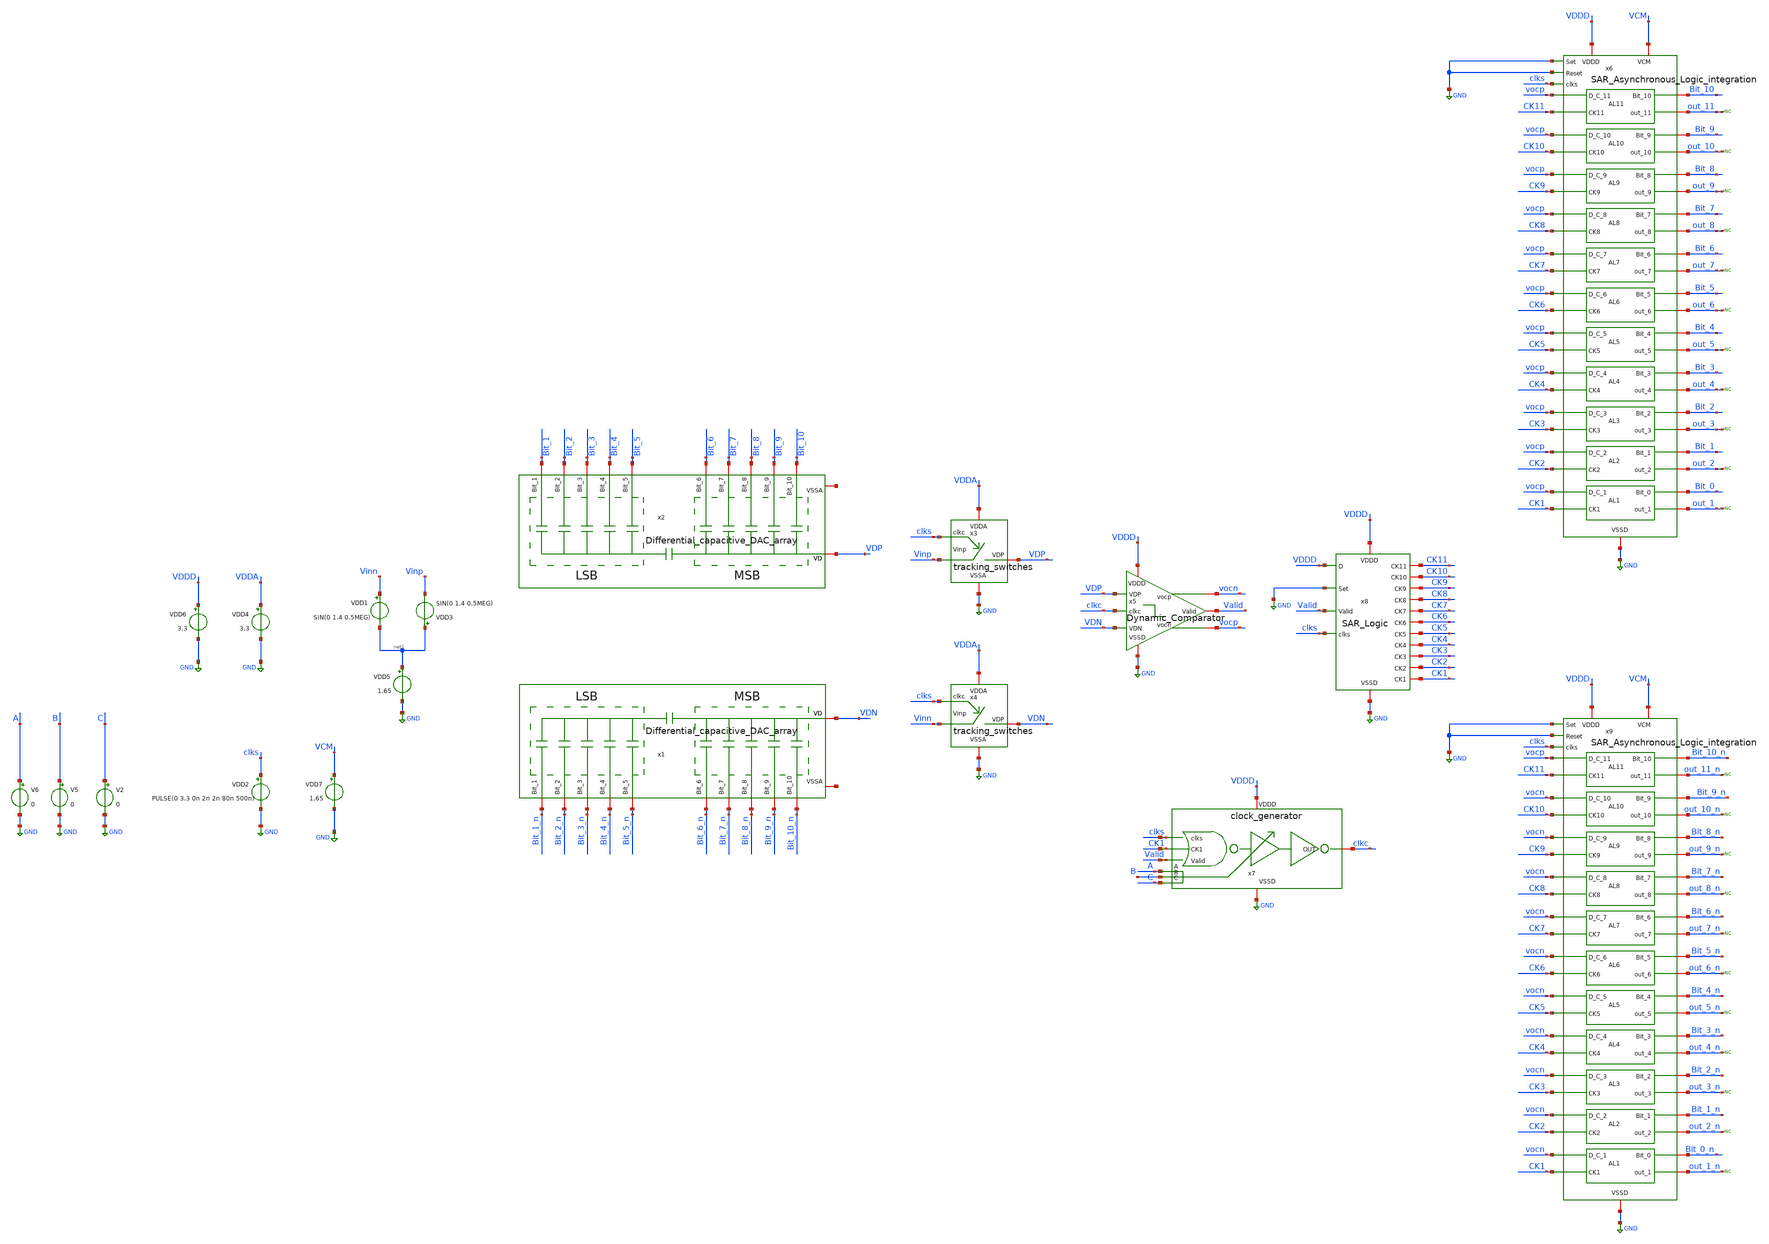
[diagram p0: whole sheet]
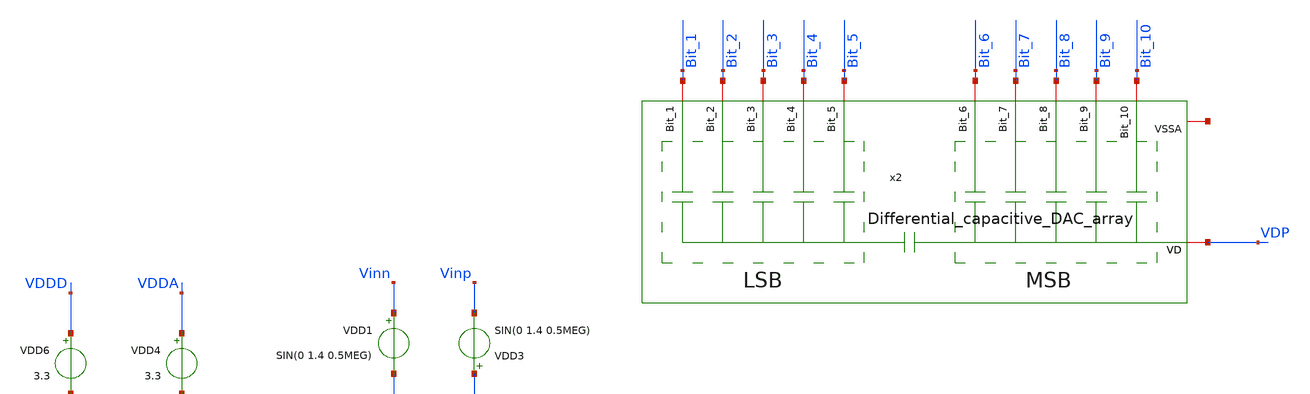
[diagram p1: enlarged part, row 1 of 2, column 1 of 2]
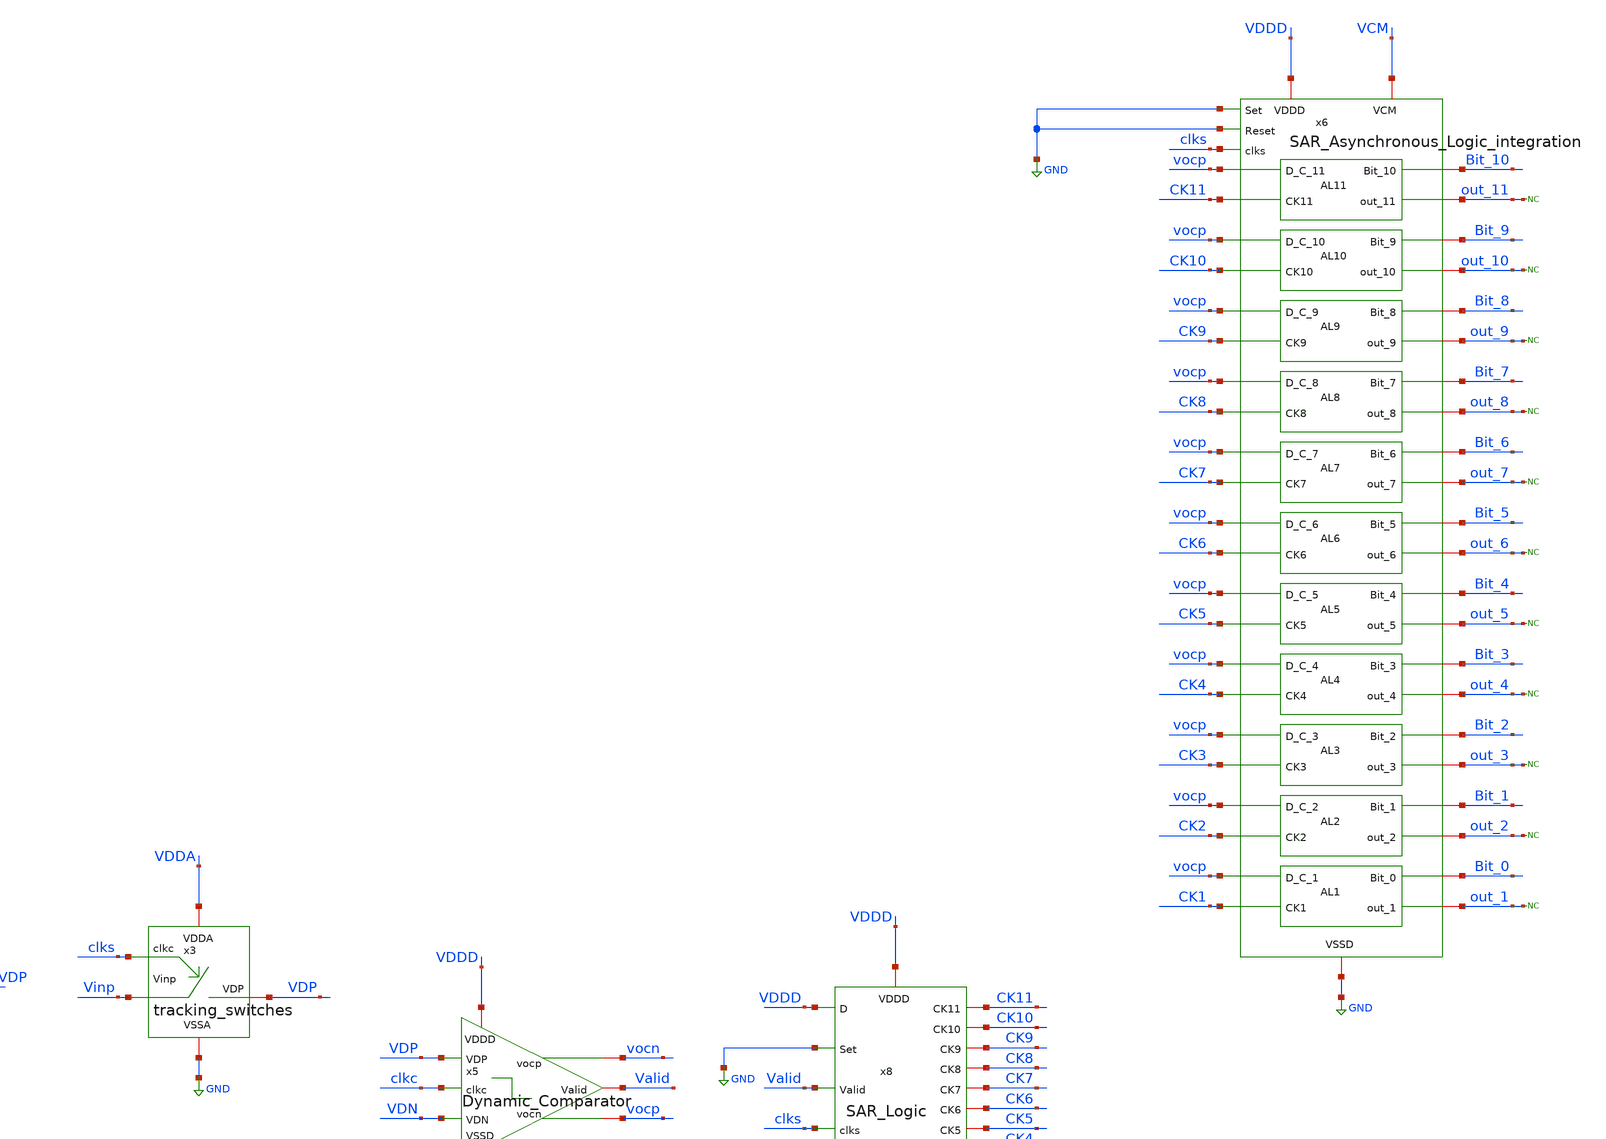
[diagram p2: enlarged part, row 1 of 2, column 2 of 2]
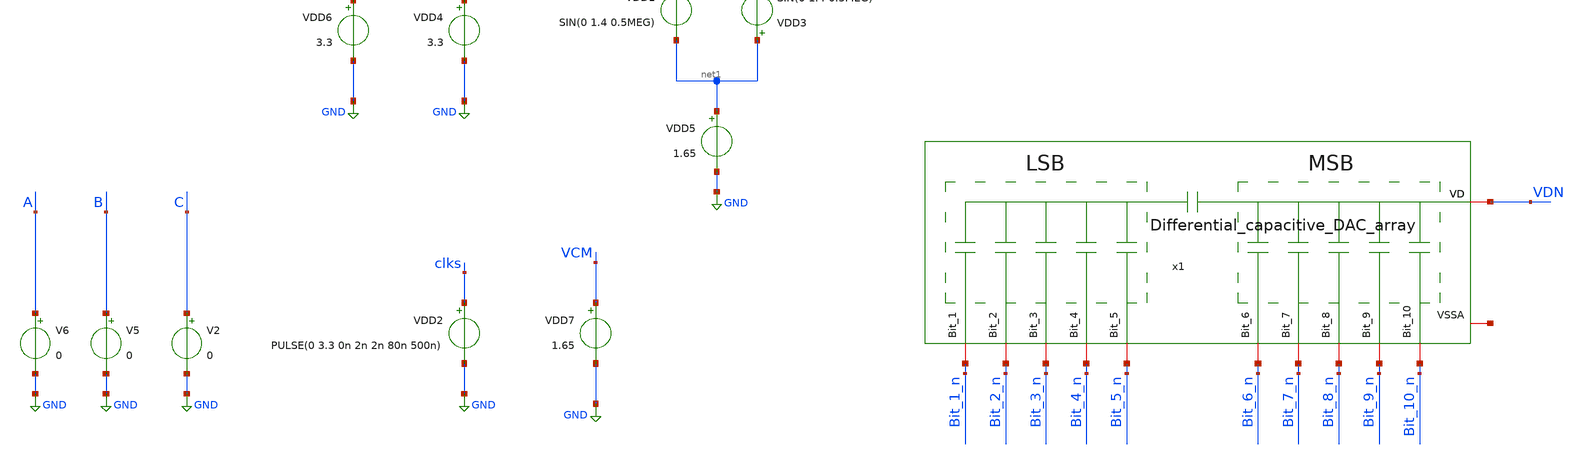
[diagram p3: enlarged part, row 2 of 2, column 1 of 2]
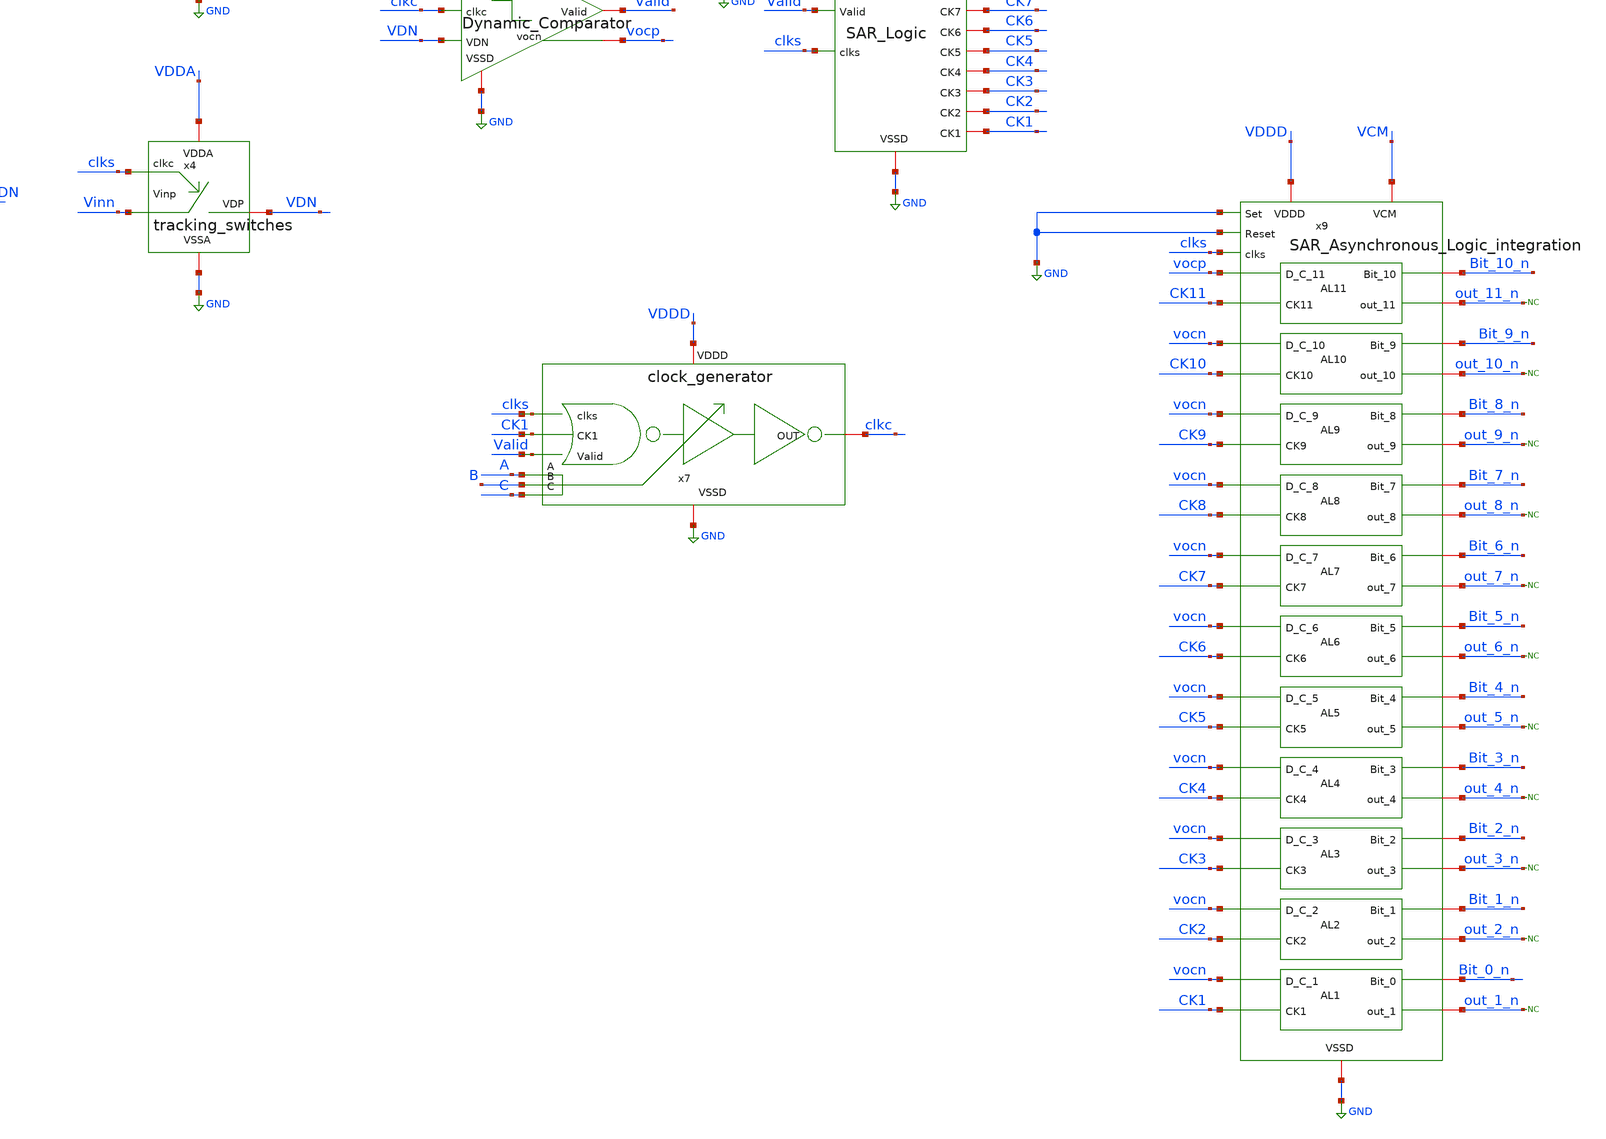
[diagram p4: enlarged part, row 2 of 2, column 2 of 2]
** sch_path: SAR_ADC/integration/integration_tb_bkp.sch
**.subckt integration_tb_bkp
x1 VDN Bit_3_n Bit_8_n Bit_5_n Bit_6_n Bit_7_n Bit_4_n Bit_9_n Bit_10_n Bit_2_n Bit_1_n net2
+ Differential_capacitive_DAC_array
x2 VDP Bit_3 Bit_8 Bit_5 Bit_6 Bit_7 Bit_4 Bit_9 Bit_10 Bit_2 Bit_1 net3
+ Differential_capacitive_DAC_array
x3 VDP VDDA GND clks Vinp tracking_switches
x4 VDN VDDA GND clks Vinn tracking_switches
x5 vocn vocp VDDD GND VDP VDN Valid clkc Dynamic_Comparator
x6 VDDD Bit_10 vocp GND CK11 VCM out_11 GND GND clks Bit_9 vocp CK10 out_10 Bit_8 vocp CK9 out_9
+ Bit_7 vocp CK8 out_8 Bit_6 vocp CK7 out_7 Bit_5 vocp CK6 out_6 Bit_4 vocp CK5 out_5 Bit_3 vocp CK4 out_4
+ Bit_2 vocp CK3 out_3 Bit_1 vocp CK2 out_2 Bit_0 vocp CK1 out_1 SAR_Asynchronous_Logic_integration
x7 clkc VDDD GND clks CK1 Valid A B C clock_generator
VDD4 VDDA GND 3.3
VDD1 Vinn net1 SIN(0 1.4 0.5MEG)
VDD3 net1 Vinp SIN(0 1.4 0.5MEG)
VDD6 VDDD GND 3.3
VDD2 clks GND PULSE(0 3.3 0n 2n 2n 80n 500n)
VDD7 VCM GND 1.65
* noconn out_11
* noconn out_10
* noconn out_9
* noconn out_8
* noconn out_7
* noconn out_6
* noconn out_5
* noconn out_4
* noconn out_3
* noconn out_2
* noconn out_1
x9 VDDD Bit_10_n vocp GND CK11 VCM out_11_n GND GND clks Bit_9_n vocn CK10 out_10_n Bit_8_n vocn CK9
+ out_9_n Bit_7_n vocn CK8 out_8_n Bit_6_n vocn CK7 out_7_n Bit_5_n vocn CK6 out_6_n Bit_4_n vocn CK5 out_5_n
+ Bit_3_n vocn CK4 out_4_n Bit_2_n vocn CK3 out_3_n Bit_1_n vocn CK2 out_2_n Bit_0_n vocn CK1 out_1_n
+ SAR_Asynchronous_Logic_integration
* noconn out_11_n
* noconn out_10_n
* noconn out_9_n
* noconn out_8_n
* noconn out_7_n
* noconn out_6_n
* noconn out_5_n
* noconn out_4_n
* noconn out_3_n
* noconn out_2_n
* noconn out_1_n
x8 CK11 VDDD CK1 CK6 GND CK10 CK5 CK9 CK4 clks CK8 CK3 Valid CK2 CK7 GND VDDD SAR_Logic
VDD5 net1 GND 1.65
V2 C GND 0
V5 B GND 0
V6 A GND 0
**** begin user architecture code



*Parameters

.options TEMP = 50.0
.lib /home/electrica/Documents/gf180_projects/pdk/gf180mcuD/libs.tech/ngspice/sm141064.ngspice typical
.lib /home/electrica/Documents/gf180_projects/pdk/gf180mcuD/libs.tech/ngspice/sm141064.ngspice cap_mim

.lib /home/electrica/Documents/gf180_projects/pdk/gf180mcuD/libs.tech/ngspice/sm141064.ngspice mimcap_statistical
.include /home/electrica/Documents/gf180_projects/pdk/gf180mcuD/libs.tech/ngspice/design.ngspice

*Data to save
.save v(Vinp)
.save v(VDP)
.save v(Vinn)
.save v(VDN)
*.save v(clkc)
*.save v(x5.aN)
*.save v(x5.aP)
*.save v(x5.dN)
*.save v(x5.dP)

.save v(clks)
*.save v(CK1)
.save v(Valid)
.save v(CK11)
.save v(CK10)
.save v(CK9)
.save v(CK8)
.save v(CK7)
.save v(CK6)
.save v(CK5)
.save v(CK4)
.save v(CK3)
.save v(CK2)
.save v(CK1)
.save v(Bit_10)
.save v(Bit_10_n)
*.save v(vocp)
*.save v(vocn)

* Simulation
.control
tran 0.1n 2u 0.01n
setplot dc1
let vout_diff = VDP-VDN
let vin_diff = Vinp-Vinn
plot v(Bit_10_n)+12 v(Bit_10)+12 v(clks)+8 v(Valid)+4 v(vin_diff) v(vout_diff)
*plot v(clks)+8 v(Vinp)+4 v(VDP)+4 v(Vinn) v(VDN)

*setplot dc2
*plot v(clks)+8 v(Vinp)+4 v(VDP)

*setplot dc3
*plot v(clkc)+20 v(VDP)+16 v(VDN)+12 v(vocp)+8 v(vocn)+4 v(Valid)

setplot dc4
plot v(Valid)+48 v(clks)+44 v(CK11)+40 v(CK10)+36 v(CK9)+32 v(CK8)+28 v(CK7)+24 v(CK6)+20 v(CK5)+16
+ v(CK4)+12 v(CK3)+8 v(CK2)+4 v(CK1)

*setplot dc1
*plot v(VDP)+20 v(VDN)+20 v(clkc)+16 v(x5.aN)+12 v(x5.aP)+8 v(x5.dP)+4 v(x5.dN)

set filetype = ascii
write integration_tb_tran.raw

reset
unset filetype
op
save all
write integration_tb.raw


.endc
.end


**** end user architecture code
**.ends
.GLOBAL GND
.end
